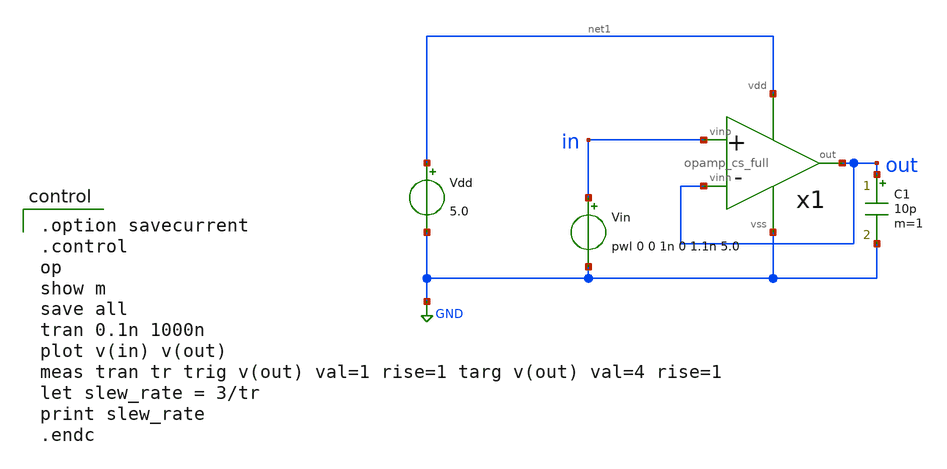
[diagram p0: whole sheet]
** sch_path: member_project/GroupWork/Team_Ando/dokunira/sch/opamp_cs_full_tran.sch
**.subckt opamp_cs_full_tran
Vdd net1 GND 5.0
C1 out GND 10p m=1
Vin in GND pwl 0 0 1n 0 1.1n 5.0
x1 in out out net1 GND opamp_cs_full
**** begin user architecture code

.option savecurrent
.control
op
show m
save all
tran 0.1n 1000n
plot v(in) v(out)
meas tran tr trig v(out) val=1 rise=1 targ v(out) val=4 rise=1
let slew_rate = 3/tr
print slew_rate
.endc

 .include $::LIB/mos.lib
.include $::LIB/passive.lib
.include $::LIB/diode.lib
**** end user architecture code
**.ends

* expanding   symbol:  opamp_cs_full.sym # of pins=5
** sym_path: member_project/GroupWork/Team_Ando/dokunira/sch/opamp_cs_full.sym
** sch_path: member_project/GroupWork/Team_Ando/dokunira/sch/opamp_cs_full.sch
.subckt opamp_cs_full vinp vinn out vdd vss
*.iopin vdd
*.iopin vss
*.ipin vinn
*.ipin vinp
*.opin out
M12 net9 net1 net6 vss nmos L=1.6u W=16u m=1
M9 net1 net3 vdd vdd pmos L=1.6u W=32u m=1
M10 net1 net1 net2 vss nmos L=1.6u W=16u m=1
M11 net2 net2 vss vss nmos L=1.6u W=16u m=1
R1 vss net4 HR_poly W=2.0 L=20
M8 net3 net3 vdd vdd pmos L=1.6u W=32u m=1
M13 net5 net3 vdd vdd pmos L=1.6u W=32u m=1
M15 net3 net5 net4 vss nmos L=1.6u W=16u m=1
M14 net5 net4 vss vss nmos L=1.6u W=16u m=1
M5 net8 net3 vdd vdd pmos L=1.6u W=64u m=1
M1 net7 vinn net8 net8 pmos L=1.6u W=128u m=1
M2 net6 vinp net8 net8 pmos L=1.6u W=128u m=1
M3 net7 net7 vss vss nmos L=1.6u W=16u m=1
M4 net6 net7 vss vss nmos L=1.6u W=16u m=1
M6 out net3 vdd vdd pmos L=1.6u W=256u m=1
M7 out net6 vss vss nmos L=1.6u W=128u m=1
C1 out net9 Poly_cap W=20 L=22
.ends

.GLOBAL GND
.end
